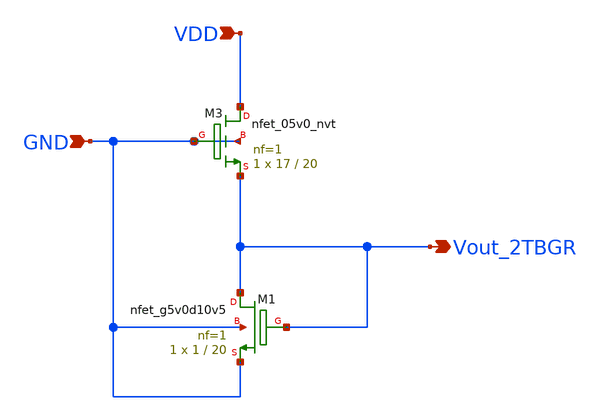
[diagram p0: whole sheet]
** sch_path: 2TBGR/Schematics/Twotran-BGR.sch
**.subckt Twotran-BGR GND VDD Vout_2TBGR
*.ipin GND
*.ipin VDD
*.opin Vout_2TBGR
XM3 VDD GND Vout_2TBGR GND sky130_fd_pr__nfet_05v0_nvt L=20 W=17 nf=1 ad='int((nf+1)/2) * W/nf * 0.29'
+ as='int((nf+2)/2) * W/nf * 0.29' pd='2*int((nf+1)/2) * (W/nf + 0.29)' ps='2*int((nf+2)/2) * (W/nf + 0.29)'
+ nrd='0.29 / W' nrs='0.29 / W' sa=0 sb=0 sd=0 mult=1 m=1
XM1 Vout_2TBGR Vout_2TBGR GND GND sky130_fd_pr__nfet_g5v0d10v5 L=20 W=1 nf=1 ad='int((nf+1)/2) * W/nf * 0.29'
+ as='int((nf+2)/2) * W/nf * 0.29' pd='2*int((nf+1)/2) * (W/nf + 0.29)' ps='2*int((nf+2)/2) * (W/nf + 0.29)'
+ nrd='0.29 / W' nrs='0.29 / W' sa=0 sb=0 sd=0 mult=1 m=1
**.ends
.end
